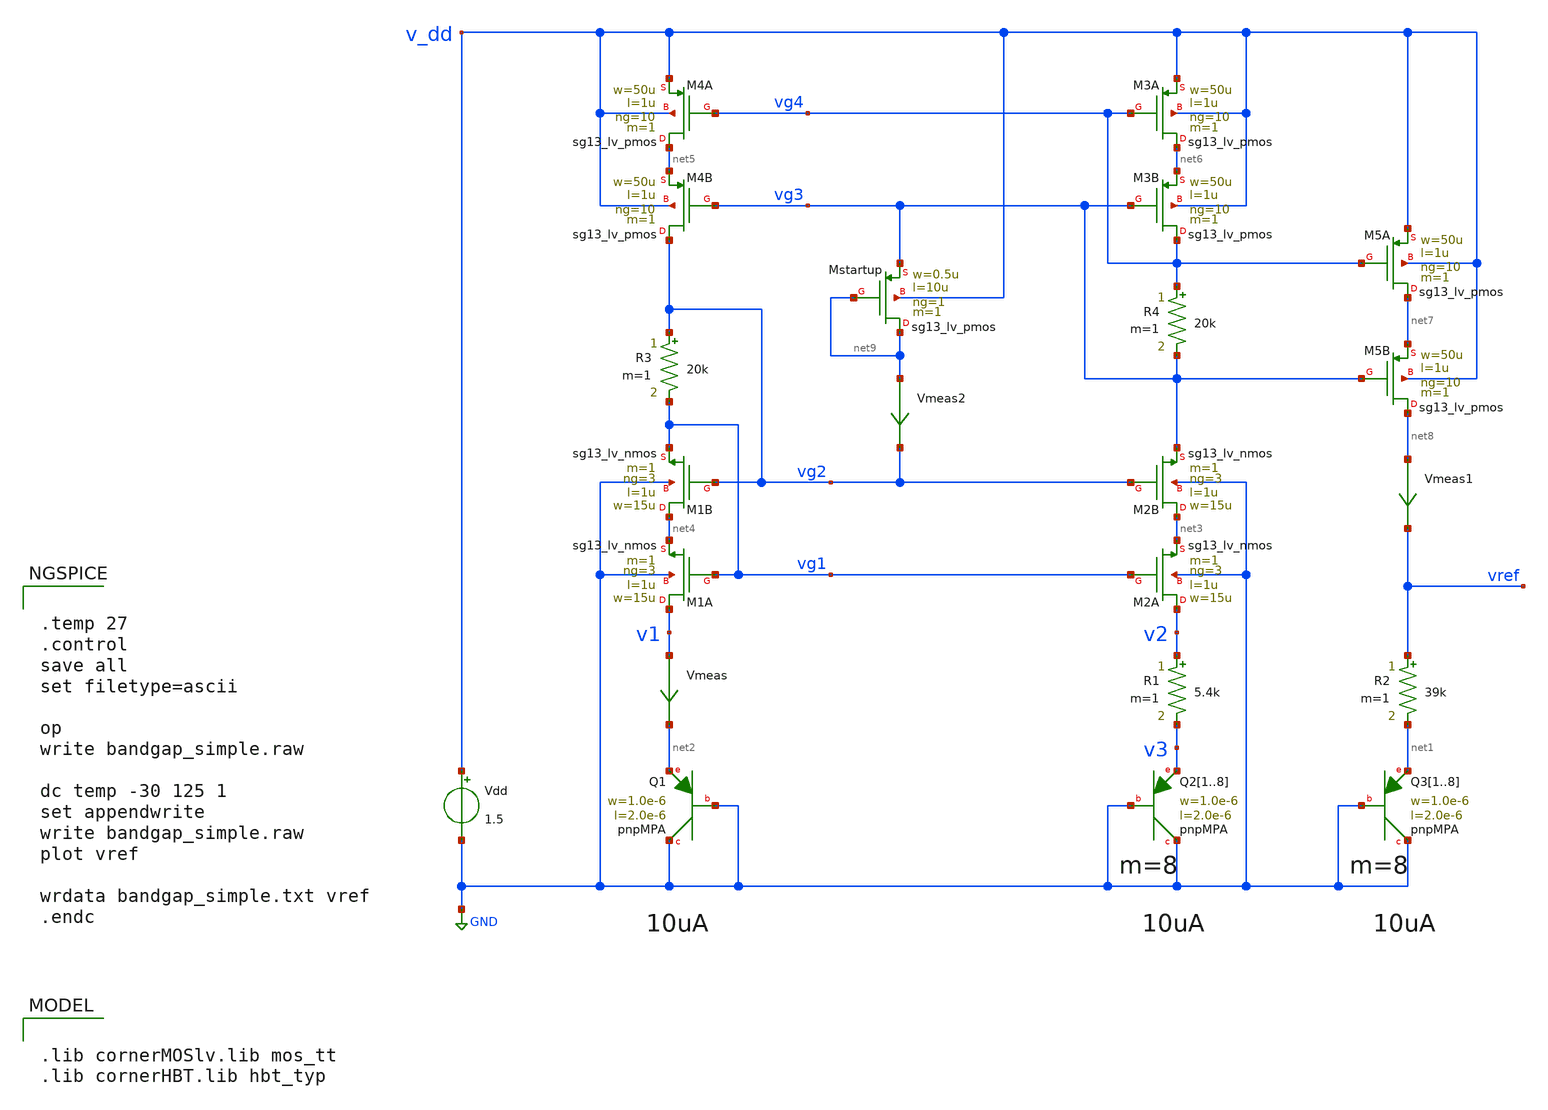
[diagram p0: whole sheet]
** sch_path: xschem/bandgap_simple.sch
* (c) 2025 H. Pretl, Apache-2.0 license
**.subckt bandgap_simple
Vdd v_dd GND 1.5
XQ1 GND GND net2 pnpMPA a=2p p=6u m=1
XQ21 GND GND v3 pnpMPA a=2p p=6u m=1
XQ22 GND GND v3 pnpMPA a=2p p=6u m=1
XQ23 GND GND v3 pnpMPA a=2p p=6u m=1
XQ24 GND GND v3 pnpMPA a=2p p=6u m=1
XQ25 GND GND v3 pnpMPA a=2p p=6u m=1
XQ26 GND GND v3 pnpMPA a=2p p=6u m=1
XQ27 GND GND v3 pnpMPA a=2p p=6u m=1
XQ28 GND GND v3 pnpMPA a=2p p=6u m=1
R1 v2 v3 5.4k m=1
XM1A v1 vg1 net4 GND sg13_lv_nmos w=15u l=1u ng=3 m=1 mm_ok=1
XQ31 GND GND net1 pnpMPA a=2p p=6u m=1
XQ32 GND GND net1 pnpMPA a=2p p=6u m=1
XQ33 GND GND net1 pnpMPA a=2p p=6u m=1
XQ34 GND GND net1 pnpMPA a=2p p=6u m=1
XQ35 GND GND net1 pnpMPA a=2p p=6u m=1
XQ36 GND GND net1 pnpMPA a=2p p=6u m=1
XQ37 GND GND net1 pnpMPA a=2p p=6u m=1
XQ38 GND GND net1 pnpMPA a=2p p=6u m=1
R2 vref net1 39k m=1
Vmeas v1 net2 0
.save i(vmeas)
Vmeas1 net8 vref 0
.save i(vmeas1)
R3 vg2 vg1 20k m=1
XM4B vg2 vg3 net5 v_dd sg13_lv_pmos w=50u l=1u ng=10 m=1 mm_ok=1
R4 vg4 vg3 20k m=1
XM1B net4 vg2 vg1 GND sg13_lv_nmos w=15u l=1u ng=3 m=1 mm_ok=1
XM2A v2 vg1 net3 GND sg13_lv_nmos w=15u l=1u ng=3 m=1 mm_ok=1
XM2B net3 vg2 vg3 GND sg13_lv_nmos w=15u l=1u ng=3 m=1 mm_ok=1
XM4A net5 vg4 v_dd v_dd sg13_lv_pmos w=50u l=1u ng=10 m=1 mm_ok=1
XM3B vg4 vg3 net6 v_dd sg13_lv_pmos w=50u l=1u ng=10 m=1 mm_ok=1
XM3A net6 vg4 v_dd v_dd sg13_lv_pmos w=50u l=1u ng=10 m=1 mm_ok=1
XM5A net7 vg4 v_dd v_dd sg13_lv_pmos w=50u l=1u ng=10 m=1 mm_ok=1
XM5B net8 vg3 net7 v_dd sg13_lv_pmos w=50u l=1u ng=10 m=1 mm_ok=1
XMstartup net9 net9 vg3 v_dd sg13_lv_pmos w=0.5u l=10u ng=1 m=1 mm_ok=1
Vmeas2 net9 vg2 0
.save i(vmeas2)
**** begin user architecture code

.lib cornerMOSlv.lib mos_tt
.lib cornerHBT.lib hbt_typ



.temp 27
.control
save all
set filetype=ascii

op
write bandgap_simple.raw

dc temp -30 125 1
set appendwrite
write bandgap_simple.raw
plot vref

wrdata bandgap_simple.txt vref
.endc


**** end user architecture code
**.ends
.GLOBAL GND
.end
